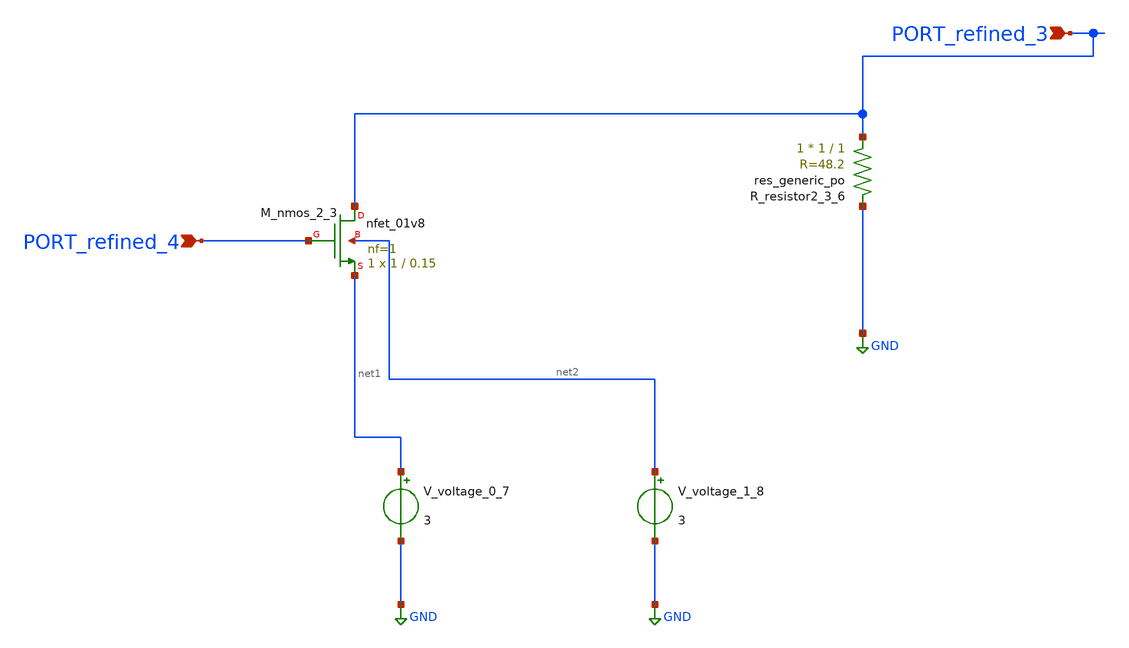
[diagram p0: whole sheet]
** sch_path: schematics/AMSNet/40.sch
**.subckt 40 PORT_refined_4 PORT_refined_3
*.ipin PORT_refined_4
*.ipin PORT_refined_3
XM_nmos_2_3 PORT_refined_3 PORT_refined_4 net1 net2 sky130_fd_pr__nfet_01v8 L=0.15 W=1 nf=1 ad='int((1 + 1)/2) * 1 / 1 * 0.29'
+ as='int((1 + 2)/2) * 1 / 1 * 0.29' pd='2*int((1 + 1)/2) * (1 / 1 + 0.29)' ps='2*int((1 + 2)/2) * (1 / 1 + 0.29)'
+ nrd='0.29 / 1 ' nrs='0.29 / 1 ' sa=0 sb=0 sd=0 mult=1 m=1
XR_resistor2_3_6 PORT_refined_3 GND sky130_fd_pr__res_generic_po W=1 L=1 m=1
V_voltage_0_7 net1 GND 3
V_voltage_1_8 net2 GND 3
**.ends
.GLOBAL GND
.end
